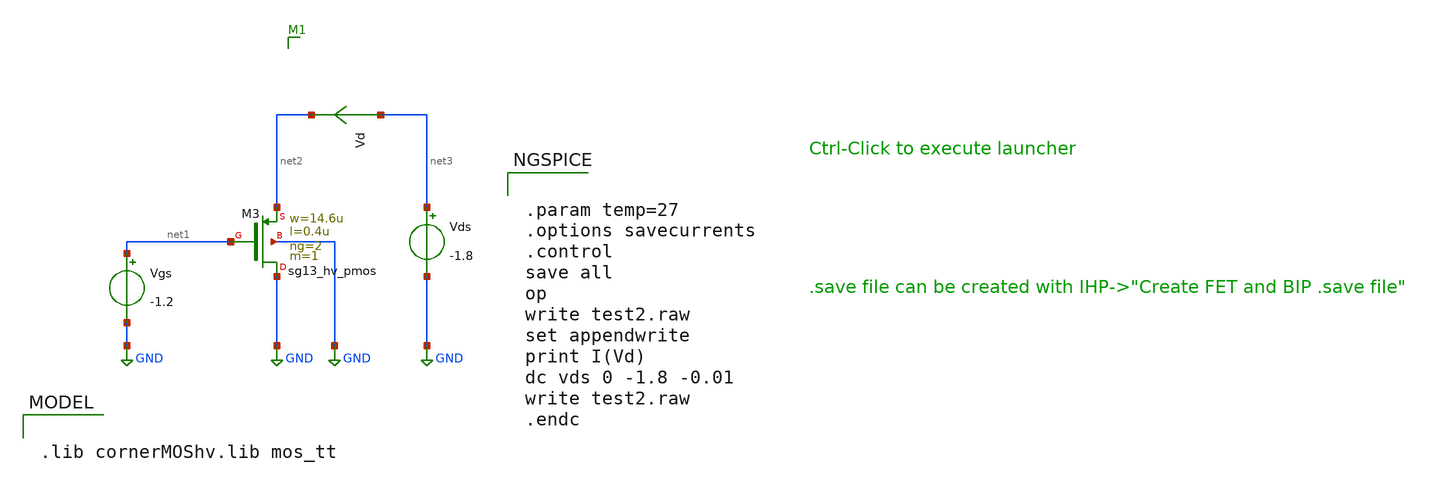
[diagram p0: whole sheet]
** sch_path: schematic/test2.sch
**.subckt test2
Vgs net1 GND -1.2
Vds net3 GND -1.8
Vd net3 net2 0
.save i(vd)
XM3 GND net1 net2 GND sg13_hv_pmos w=14.6u l=0.4u ng=2 m=1 mm_ok=1
**** begin user architecture code

.lib cornerMOShv.lib mos_tt



.param temp=27
.options savecurrents
.control
save all
op
write test2.raw
set appendwrite
print I(Vd)
dc vds 0 -1.8 -0.01
write test2.raw
.endc


**** end user architecture code
**.ends
.GLOBAL GND
.end
